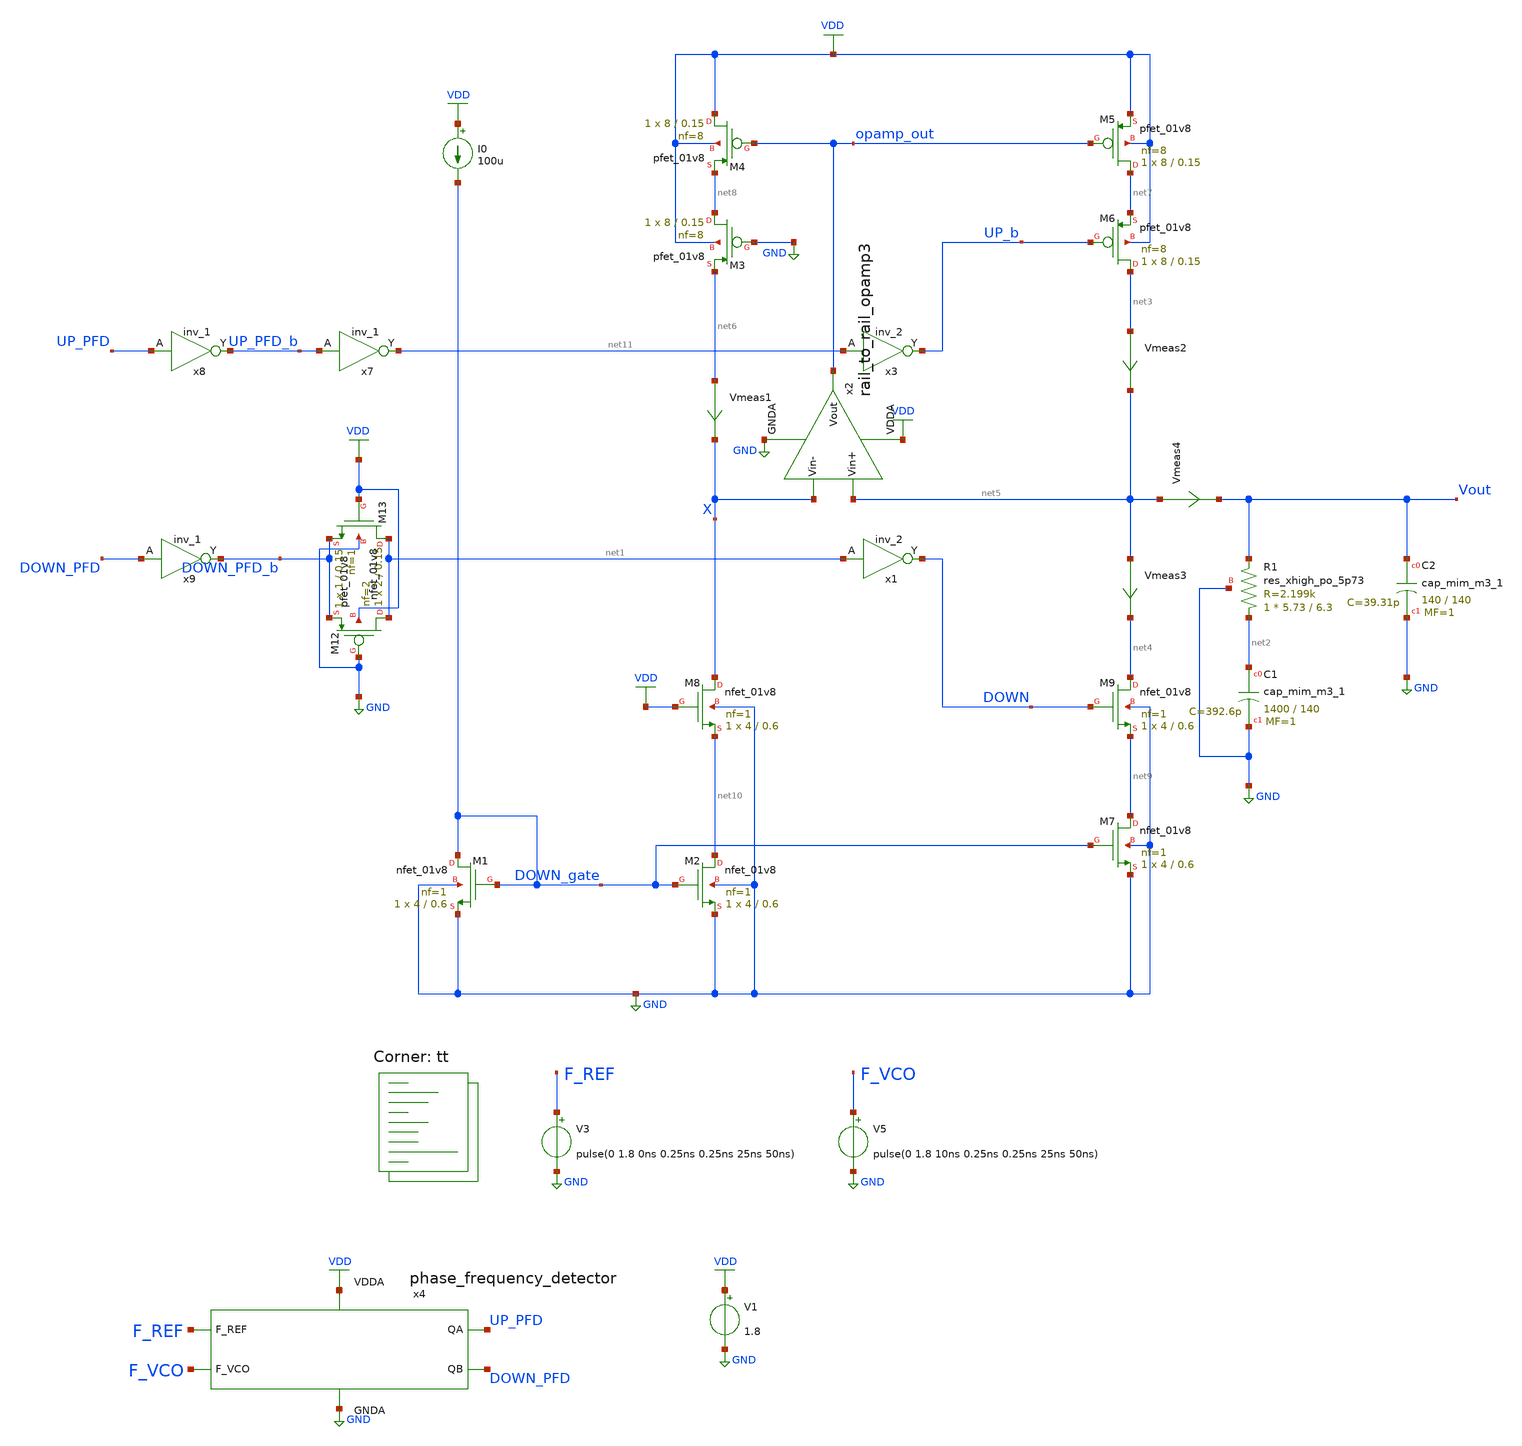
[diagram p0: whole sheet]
** sch_path: projects/pll/charge_pump/xschem_ngspice/pfd_charge_pump_4.sch
**.subckt pfd_charge_pump_4
V1 VDD GND 1.8
XM12 net1 GND DOWN_PFD_b VDD sky130_fd_pr__pfet_01v8 L=0.15 W=2 nf=2 ad='int((nf+1)/2) * W/nf * 0.29'
+ as='int((nf+2)/2) * W/nf * 0.29' pd='2*int((nf+1)/2) * (W/nf + 0.29)' ps='2*int((nf+2)/2) * (W/nf + 0.29)'
+ nrd='0.29 / W' nrs='0.29 / W' sa=0 sb=0 sd=0 mult=1 m=1
XM13 net1 VDD DOWN_PFD_b GND sky130_fd_pr__nfet_01v8 L=0.15 W=1 nf=1 ad='int((nf+1)/2) * W/nf * 0.29'
+ as='int((nf+2)/2) * W/nf * 0.29' pd='2*int((nf+1)/2) * (W/nf + 0.29)' ps='2*int((nf+2)/2) * (W/nf + 0.29)'
+ nrd='0.29 / W' nrs='0.29 / W' sa=0 sb=0 sd=0 mult=1 m=1
x7 UP_PFD_b GND GND VDD VDD net11 sky130_fd_sc_hd__inv_1
x8 UP_PFD GND GND VDD VDD UP_PFD_b sky130_fd_sc_hd__inv_1
x9 DOWN_PFD GND GND VDD VDD DOWN_PFD_b sky130_fd_sc_hd__inv_1
XC2 Vout GND sky130_fd_pr__cap_mim_m3_1 W=140 L=140 MF=1 m=1
XC1 net2 GND sky130_fd_pr__cap_mim_m3_1 W=1400 L=140 MF=1 m=1
V3 F_REF GND pulse(0 1.8 0ns 0.25ns 0.25ns 25ns 50ns)
V5 F_VCO GND pulse(0 1.8 10ns 0.25ns 0.25ns 25ns 50ns)
x4 F_REF F_VCO VDD UP_PFD DOWN_PFD GND phase_frequency_detector
XR1 net2 Vout GND sky130_fd_pr__res_xhigh_po_5p73 L=6.3 mult=1 m=1
XM1 DOWN_gate DOWN_gate GND GND sky130_fd_pr__nfet_01v8 L=0.6 W=4 nf=1 ad='int((nf+1)/2) * W/nf * 0.29'
+ as='int((nf+2)/2) * W/nf * 0.29' pd='2*int((nf+1)/2) * (W/nf + 0.29)' ps='2*int((nf+2)/2) * (W/nf + 0.29)'
+ nrd='0.29 / W' nrs='0.29 / W' sa=0 sb=0 sd=0 mult=1 m=1
XM2 net10 DOWN_gate GND GND sky130_fd_pr__nfet_01v8 L=0.6 W=4 nf=1 ad='int((nf+1)/2) * W/nf * 0.29' as='int((nf+2)/2) * W/nf * 0.29'
+ pd='2*int((nf+1)/2) * (W/nf + 0.29)' ps='2*int((nf+2)/2) * (W/nf + 0.29)' nrd='0.29 / W' nrs='0.29 / W'
+ sa=0 sb=0 sd=0 mult=1 m=1
XM3 net8 GND net6 VDD sky130_fd_pr__pfet_01v8 L=0.15 W=8 nf=8 ad='int((nf+1)/2) * W/nf * 0.29' as='int((nf+2)/2) * W/nf * 0.29'
+ pd='2*int((nf+1)/2) * (W/nf + 0.29)' ps='2*int((nf+2)/2) * (W/nf + 0.29)' nrd='0.29 / W' nrs='0.29 / W'
+ sa=0 sb=0 sd=0 mult=1 m=1
I0 VDD DOWN_gate 100u
Vmeas1 net6 X 0
.save i(vmeas1)
XM5 net7 opamp_out VDD VDD sky130_fd_pr__pfet_01v8 L=0.15 W=8 nf=8 ad='int((nf+1)/2) * W/nf * 0.29' as='int((nf+2)/2) * W/nf * 0.29'
+ pd='2*int((nf+1)/2) * (W/nf + 0.29)' ps='2*int((nf+2)/2) * (W/nf + 0.29)' nrd='0.29 / W' nrs='0.29 / W'
+ sa=0 sb=0 sd=0 mult=1 m=1
XM6 net3 UP_b net7 VDD sky130_fd_pr__pfet_01v8 L=0.15 W=8 nf=8 ad='int((nf+1)/2) * W/nf * 0.29' as='int((nf+2)/2) * W/nf * 0.29'
+ pd='2*int((nf+1)/2) * (W/nf + 0.29)' ps='2*int((nf+2)/2) * (W/nf + 0.29)' nrd='0.29 / W' nrs='0.29 / W'
+ sa=0 sb=0 sd=0 mult=1 m=1
Vmeas2 net3 net5 0
.save i(vmeas2)
Vmeas3 net5 net4 0
.save i(vmeas3)
XM9 net4 DOWN net9 GND sky130_fd_pr__nfet_01v8 L=0.6 W=4 nf=1 ad='int((nf+1)/2) * W/nf * 0.29' as='int((nf+2)/2) * W/nf * 0.29'
+ pd='2*int((nf+1)/2) * (W/nf + 0.29)' ps='2*int((nf+2)/2) * (W/nf + 0.29)' nrd='0.29 / W' nrs='0.29 / W'
+ sa=0 sb=0 sd=0 mult=1 m=1
x3 net11 GND GND VDD VDD UP_b sky130_fd_sc_hd__inv_2
x1 net1 GND GND VDD VDD DOWN sky130_fd_sc_hd__inv_2
x2 VDD net5 X opamp_out GND rail_to_rail_opamp3
XM4 VDD opamp_out net8 VDD sky130_fd_pr__pfet_01v8 L=0.15 W=8 nf=8 ad='int((nf+1)/2) * W/nf * 0.29' as='int((nf+2)/2) * W/nf * 0.29'
+ pd='2*int((nf+1)/2) * (W/nf + 0.29)' ps='2*int((nf+2)/2) * (W/nf + 0.29)' nrd='0.29 / W' nrs='0.29 / W'
+ sa=0 sb=0 sd=0 mult=1 m=1
XM7 net9 DOWN_gate GND GND sky130_fd_pr__nfet_01v8 L=0.6 W=4 nf=1 ad='int((nf+1)/2) * W/nf * 0.29' as='int((nf+2)/2) * W/nf * 0.29'
+ pd='2*int((nf+1)/2) * (W/nf + 0.29)' ps='2*int((nf+2)/2) * (W/nf + 0.29)' nrd='0.29 / W' nrs='0.29 / W'
+ sa=0 sb=0 sd=0 mult=1 m=1
XM8 X VDD net10 GND sky130_fd_pr__nfet_01v8 L=0.6 W=4 nf=1 ad='int((nf+1)/2) * W/nf * 0.29' as='int((nf+2)/2) * W/nf * 0.29'
+ pd='2*int((nf+1)/2) * (W/nf + 0.29)' ps='2*int((nf+2)/2) * (W/nf + 0.29)' nrd='0.29 / W' nrs='0.29 / W'
+ sa=0 sb=0 sd=0 mult=1 m=1
Vmeas4 net5 Vout 0
.save i(vmeas4)
**** begin user architecture code
.lib $::SKYWATER_MODELS/sky130.lib.spice tt



.include /foss/pdks/sky130A/libs.ref/sky130_fd_sc_hd/spice/sky130_fd_sc_hd.spice

.option method=gear trtol1
.option wnflag=1
* .option savecurrents

* .temp = 75

.ic v(vout) = 1.2

.save  v(up_pfd) v(down_pfd) v(up_pfd_b) v(down_pfd_b) v(up) v(up_b) v(down) v(down_b) v(v2) v(x) v(y) v(z) v(vout) v(up_input) v(down_input) v(down_gate) v(opamp_out) v(x2.p_bias) v(x2.n_bias) v(x2.v_common_p) v(x2.v_common_n) v(x2.p_left) v(x2.p_right) v(x2.n_left) v(x2.n_right) v(f_ref) v(f_vco) v(x4.qa) v(x4.qa_b) v(x4.qb) v(x4.qb_b) v(x4.qa) v(x4.e) v(x4.e_b) v(x4.f) v(x4.f_b) v(x4.before_reset) v(x4.reset)


.control
  * save v(up_pfd) v(down_pfd) v(up_pfd_b) v(down_pfd_b) v(up) v(up_b) v(down) v(down_b) v(x)
+ v(vout) v(up_input) v(down_input)
  * save all

  tran 1ns 10us
  * dc v2 0 1.8 0.01
  remzerovec
  write pfd_charge_pump_4.raw
  * wrdata /foss/designs/my_design/projects/pll/pfd/xschem_ngspice/charge_pump2_QA.txt v(osc)
  set appendwrite

.endc






**** end user architecture code
**.ends

* expanding   symbol:
*+  /foss/designs/my_design/projects/pll/pfd/xschem_ngspice/phase_frequency_detector.sym # of pins=6
** sym_path: projects/pll/pfd/xschem_ngspice/phase_frequency_detector.sym
** sch_path: projects/pll/pfd/xschem_ngspice/phase_frequency_detector.sch
.subckt phase_frequency_detector F_REF F_VCO VDDA QA QB GNDA
*.ipin F_REF
*.opin QA
*.ipin F_VCO
*.opin QB
*.ipin VDDA
*.ipin GNDA
x1 F_REF QA GNDA GNDA VDDA VDDA QA_b sky130_fd_sc_hd__nor2_1
x2 QA_b E GNDA GNDA VDDA VDDA QA sky130_fd_sc_hd__nor2_1
x3 QA_b E_b GNDA GNDA VDDA VDDA E sky130_fd_sc_hd__nor2_1
x4 E Reset GNDA GNDA VDDA VDDA E_b sky130_fd_sc_hd__nor2_1
x5 F_VCO QB GNDA GNDA VDDA VDDA QB_b sky130_fd_sc_hd__nor2_1
x6 QB_b F GNDA GNDA VDDA VDDA QB sky130_fd_sc_hd__nor2_1
x7 QB_b F_b GNDA GNDA VDDA VDDA F sky130_fd_sc_hd__nor2_1
x8 F Reset GNDA GNDA VDDA VDDA F_b sky130_fd_sc_hd__nor2_1
x9 QA QB GNDA GNDA VDDA VDDA before_Reset sky130_fd_sc_hd__nand2_1
x10 before_Reset GNDA GNDA VDDA VDDA net1 sky130_fd_sc_hd__inv_1
x11 net1 GNDA GNDA VDDA VDDA net2 sky130_fd_sc_hd__inv_1
x12 net2 GNDA GNDA VDDA VDDA net3 sky130_fd_sc_hd__inv_1
x13 net3 GNDA GNDA VDDA VDDA net4 sky130_fd_sc_hd__inv_1
x14 net4 GNDA GNDA VDDA VDDA Reset sky130_fd_sc_hd__inv_1
.ends


* expanding   symbol:
*+  /foss/designs/my_design/projects/pll/charge_pump/xschem_ngspice/rail_to_rail_opamp3.sym # of pins=5
** sym_path: projects/pll/charge_pump/xschem_ngspice/rail_to_rail_opamp3.sym
** sch_path: projects/pll/charge_pump/xschem_ngspice/rail_to_rail_opamp3.sch
.subckt rail_to_rail_opamp3 VDDA Vin+ Vin- Vout GNDA
*.opin Vout
*.ipin Vin+
*.ipin Vin-
*.ipin VDDA
*.ipin GNDA
XM2 n_left Vin+ v_common_n GNDA sky130_fd_pr__nfet_01v8 L=0.15 W=1 nf=1 ad='int((nf+1)/2) * W/nf * 0.29'
+ as='int((nf+2)/2) * W/nf * 0.29' pd='2*int((nf+1)/2) * (W/nf + 0.29)' ps='2*int((nf+2)/2) * (W/nf + 0.29)'
+ nrd='0.29 / W' nrs='0.29 / W' sa=0 sb=0 sd=0 mult=1 m=1
XM3 n_right Vin- v_common_n GNDA sky130_fd_pr__nfet_01v8 L=0.15 W=1 nf=1 ad='int((nf+1)/2) * W/nf * 0.29'
+ as='int((nf+2)/2) * W/nf * 0.29' pd='2*int((nf+1)/2) * (W/nf + 0.29)' ps='2*int((nf+2)/2) * (W/nf + 0.29)'
+ nrd='0.29 / W' nrs='0.29 / W' sa=0 sb=0 sd=0 mult=1 m=1
XM5 n_left n_left VDDA VDDA sky130_fd_pr__pfet_01v8 L=0.15 W=2 nf=2 ad='int((nf+1)/2) * W/nf * 0.29'
+ as='int((nf+2)/2) * W/nf * 0.29' pd='2*int((nf+1)/2) * (W/nf + 0.29)' ps='2*int((nf+2)/2) * (W/nf + 0.29)'
+ nrd='0.29 / W' nrs='0.29 / W' sa=0 sb=0 sd=0 mult=1 m=1
XM4 n_right n_left VDDA VDDA sky130_fd_pr__pfet_01v8 L=0.15 W=2 nf=2 ad='int((nf+1)/2) * W/nf * 0.29'
+ as='int((nf+2)/2) * W/nf * 0.29' pd='2*int((nf+1)/2) * (W/nf + 0.29)' ps='2*int((nf+2)/2) * (W/nf + 0.29)'
+ nrd='0.29 / W' nrs='0.29 / W' sa=0 sb=0 sd=0 mult=1 m=1
XM6 v_common_p p_bias VDDA VDDA sky130_fd_pr__pfet_01v8 L=0.15 W=3 nf=3 ad='int((nf+1)/2) * W/nf * 0.29'
+ as='int((nf+2)/2) * W/nf * 0.29' pd='2*int((nf+1)/2) * (W/nf + 0.29)' ps='2*int((nf+2)/2) * (W/nf + 0.29)'
+ nrd='0.29 / W' nrs='0.29 / W' sa=0 sb=0 sd=0 mult=1 m=1
XM7 p_left Vin+ v_common_p VDDA sky130_fd_pr__pfet_01v8 L=0.15 W=2 nf=2 ad='int((nf+1)/2) * W/nf * 0.29'
+ as='int((nf+2)/2) * W/nf * 0.29' pd='2*int((nf+1)/2) * (W/nf + 0.29)' ps='2*int((nf+2)/2) * (W/nf + 0.29)'
+ nrd='0.29 / W' nrs='0.29 / W' sa=0 sb=0 sd=0 mult=1 m=1
XM8 p_right Vin- v_common_p VDDA sky130_fd_pr__pfet_01v8 L=0.15 W=2 nf=2 ad='int((nf+1)/2) * W/nf * 0.29'
+ as='int((nf+2)/2) * W/nf * 0.29' pd='2*int((nf+1)/2) * (W/nf + 0.29)' ps='2*int((nf+2)/2) * (W/nf + 0.29)'
+ nrd='0.29 / W' nrs='0.29 / W' sa=0 sb=0 sd=0 mult=1 m=1
XM9 p_left p_left GNDA GNDA sky130_fd_pr__nfet_01v8 L=0.15 W=1 nf=1 ad='int((nf+1)/2) * W/nf * 0.29'
+ as='int((nf+2)/2) * W/nf * 0.29' pd='2*int((nf+1)/2) * (W/nf + 0.29)' ps='2*int((nf+2)/2) * (W/nf + 0.29)'
+ nrd='0.29 / W' nrs='0.29 / W' sa=0 sb=0 sd=0 mult=1 m=1
XM10 p_right p_left GNDA GNDA sky130_fd_pr__nfet_01v8 L=0.15 W=1 nf=1 ad='int((nf+1)/2) * W/nf * 0.29'
+ as='int((nf+2)/2) * W/nf * 0.29' pd='2*int((nf+1)/2) * (W/nf + 0.29)' ps='2*int((nf+2)/2) * (W/nf + 0.29)'
+ nrd='0.29 / W' nrs='0.29 / W' sa=0 sb=0 sd=0 mult=1 m=1
XM1 v_common_n n_bias GNDA GNDA sky130_fd_pr__nfet_01v8 L=0.15 W=1 nf=1 ad='int((nf+1)/2) * W/nf * 0.29'
+ as='int((nf+2)/2) * W/nf * 0.29' pd='2*int((nf+1)/2) * (W/nf + 0.29)' ps='2*int((nf+2)/2) * (W/nf + 0.29)'
+ nrd='0.29 / W' nrs='0.29 / W' sa=0 sb=0 sd=0 mult=1 m=1
XM11 Vout n_right VDDA VDDA sky130_fd_pr__pfet_01v8 L=0.15 W=16 nf=2 ad='int((nf+1)/2) * W/nf * 0.29'
+ as='int((nf+2)/2) * W/nf * 0.29' pd='2*int((nf+1)/2) * (W/nf + 0.29)' ps='2*int((nf+2)/2) * (W/nf + 0.29)'
+ nrd='0.29 / W' nrs='0.29 / W' sa=0 sb=0 sd=0 mult=1 m=1
XM12 Vout p_right GNDA GNDA sky130_fd_pr__nfet_01v8 L=0.15 W=8 nf=1 ad='int((nf+1)/2) * W/nf * 0.29'
+ as='int((nf+2)/2) * W/nf * 0.29' pd='2*int((nf+1)/2) * (W/nf + 0.29)' ps='2*int((nf+2)/2) * (W/nf + 0.29)'
+ nrd='0.29 / W' nrs='0.29 / W' sa=0 sb=0 sd=0 mult=1 m=1
XM13 n_bias n_bias GNDA GNDA sky130_fd_pr__nfet_01v8 L=0.15 W=1 nf=1 ad='int((nf+1)/2) * W/nf * 0.29'
+ as='int((nf+2)/2) * W/nf * 0.29' pd='2*int((nf+1)/2) * (W/nf + 0.29)' ps='2*int((nf+2)/2) * (W/nf + 0.29)'
+ nrd='0.29 / W' nrs='0.29 / W' sa=0 sb=0 sd=0 mult=1 m=1
XM15 p_bias p_bias VDDA VDDA sky130_fd_pr__pfet_01v8 L=0.15 W=2 nf=2 ad='int((nf+1)/2) * W/nf * 0.29'
+ as='int((nf+2)/2) * W/nf * 0.29' pd='2*int((nf+1)/2) * (W/nf + 0.29)' ps='2*int((nf+2)/2) * (W/nf + 0.29)'
+ nrd='0.29 / W' nrs='0.29 / W' sa=0 sb=0 sd=0 mult=1 m=1
Vmeas net1 n_bias 0
.save i(vmeas)
XM14 net1 net1 p_bias p_bias sky130_fd_pr__pfet_01v8 L=0.15 W=2 nf=2 ad='int((nf+1)/2) * W/nf * 0.29'
+ as='int((nf+2)/2) * W/nf * 0.29' pd='2*int((nf+1)/2) * (W/nf + 0.29)' ps='2*int((nf+2)/2) * (W/nf + 0.29)'
+ nrd='0.29 / W' nrs='0.29 / W' sa=0 sb=0 sd=0 mult=1 m=1
.ends

.GLOBAL GND
.GLOBAL VDD
.end
